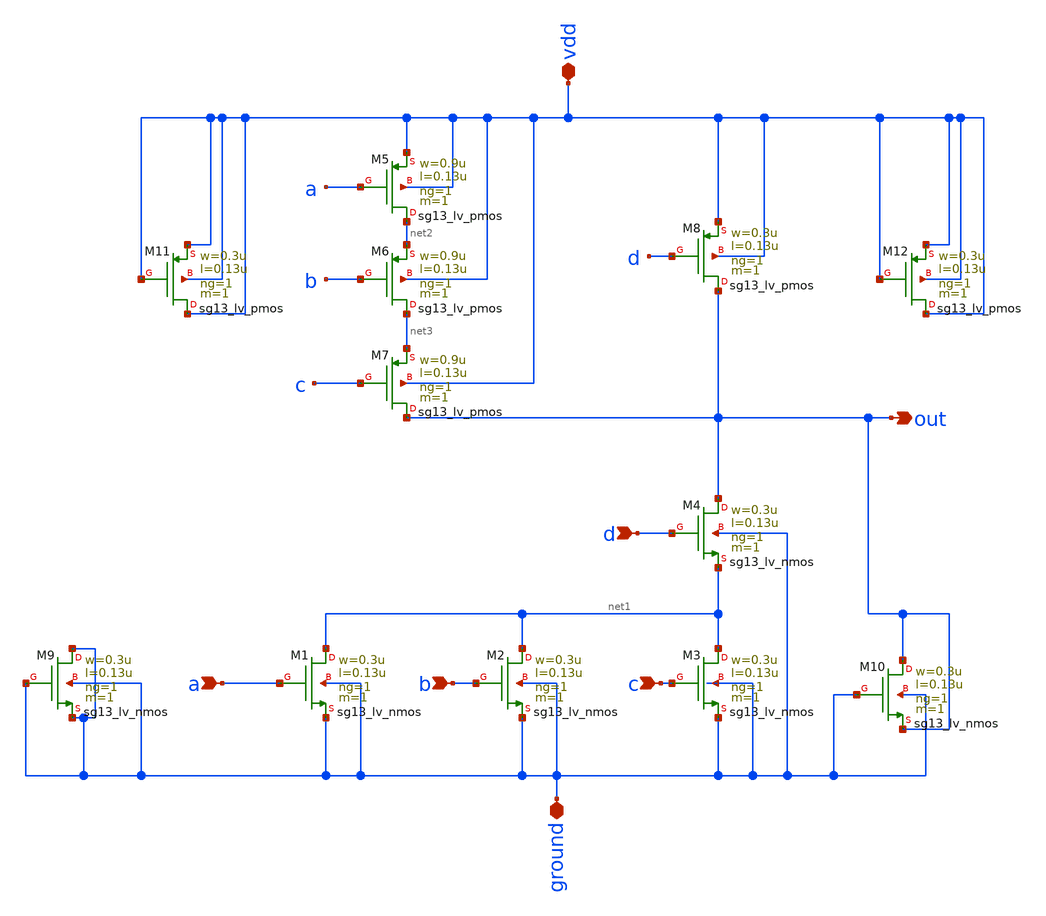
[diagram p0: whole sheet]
** sch_path: projekat/slucaj_2/schematic/funkcija_matching.sch
**.subckt funkcija_matching a b c d vdd ground out
*.ipin a
*.ipin b
*.ipin c
*.ipin d
*.iopin vdd
*.iopin ground
*.opin out
XM1 net1 a ground ground sg13_lv_nmos w=0.3u l=0.13u ng=1 m=1 mm_ok=1
XM2 net1 b ground ground sg13_lv_nmos w=0.3u l=0.13u ng=1 m=1 mm_ok=1
XM3 net1 c ground ground sg13_lv_nmos w=0.3u l=0.13u ng=1 m=1 mm_ok=1
XM4 out d net1 ground sg13_lv_nmos w=0.3u l=0.13u ng=1 m=1 mm_ok=1
XM5 net2 a vdd vdd sg13_lv_pmos w=0.9u l=0.13u ng=1 m=1 mm_ok=1
XM6 net3 b net2 vdd sg13_lv_pmos w=0.9u l=0.13u ng=1 m=1 mm_ok=1
XM7 out c net3 vdd sg13_lv_pmos w=0.9u l=0.13u ng=1 m=1 mm_ok=1
XM8 out d vdd vdd sg13_lv_pmos w=0.3u l=0.13u ng=1 m=1 mm_ok=1
XM9 ground ground ground ground sg13_lv_nmos w=0.3u l=0.13u ng=1 m=1 mm_ok=1
XM10 out ground out ground sg13_lv_nmos w=0.3u l=0.13u ng=1 m=1 mm_ok=1
XM11 vdd vdd vdd vdd sg13_lv_pmos w=0.3u l=0.13u ng=1 m=1 mm_ok=1
XM12 vdd vdd vdd vdd sg13_lv_pmos w=0.3u l=0.13u ng=1 m=1 mm_ok=1
**.ends
.end
